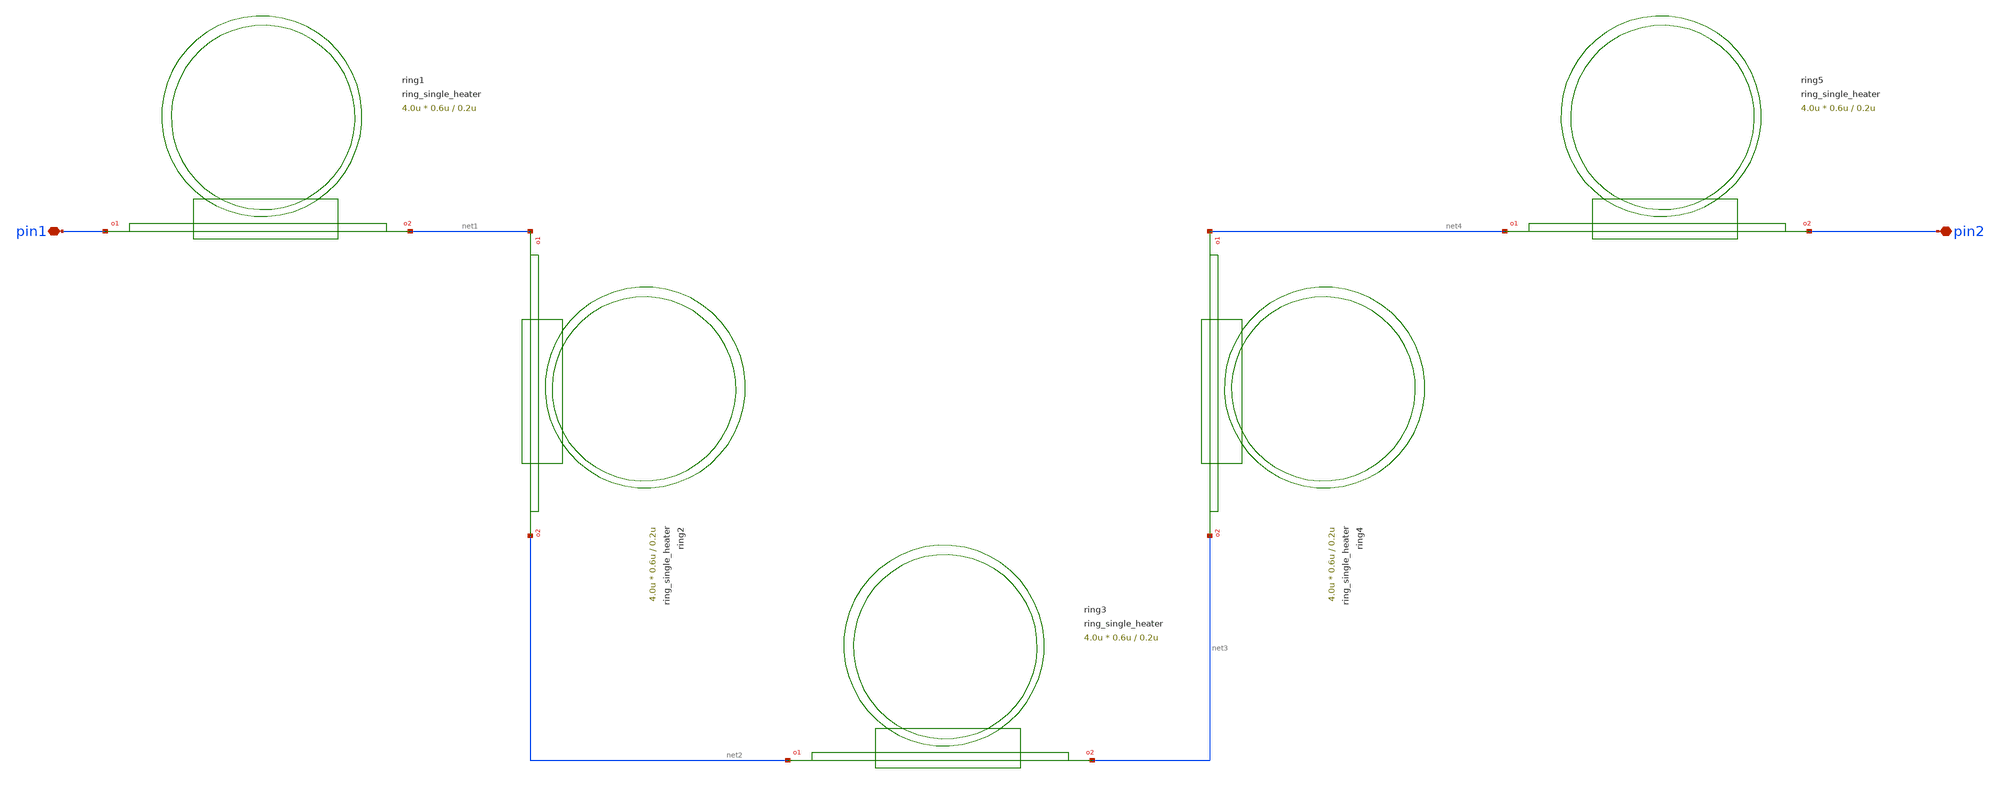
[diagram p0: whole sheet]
** sch_path: xschem/tests/test_sch/test_ring_single_heater.sch
* Copyright (c) 2024, Mabrains LLC
* Licensed under the GNU Lesser General Public License, Version 3.0 (the "License");
* you may not use this file except in compliance with the License.
* GNU Lesser General Public License
* Version 3, 29 June 2007
* This program is free software: you can redistribute it and/or modify
* it under the terms of the GNU Lesser General Public License as published
* by the Free Software Foundation, either version 3 of the License, or
* (at your option) any later version.
* This program is distributed in the hope that it will be useful,
* but WITHOUT ANY WARRANTY; without even the implied warranty of
* MERCHANTABILITY or FITNESS FOR A PARTICULAR PURPOSE.  See the
* GNU Lesser General Public License for more details.
* You should have received a copy of the GNU Lesser General Public License
* along with this program.  If not, see <https://www.gnu.org/licenses/>.
* SPDX-License-Identifier: LGPL-3.0
**.subckt test_ring_single_heater pin1 pin2
*.iopin pin1
*.iopin pin2
Pring1 pin1 net1 ring_single_heater gap=0.2u radius=10.0u length_x=4.0u length_y=0.6u
Pring3 net2 net3 ring_single_heater gap=0.2u radius=10.0u length_x=4.0u length_y=0.6u
Pring5 net4 pin2 ring_single_heater gap=0.2u radius=10.0u length_x=4.0u length_y=0.6u
Pring2 net1 net2 ring_single_heater gap=0.2u radius=10.0u length_x=4.0u length_y=0.6u
Pring4 net4 net3 ring_single_heater gap=0.2u radius=10.0u length_x=4.0u length_y=0.6u
**.ends
.end
